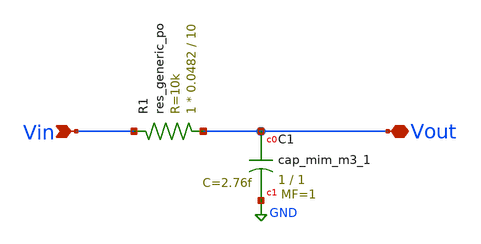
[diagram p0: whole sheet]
** sch_path: xschem/analog_desing/Filtro/LowPassFilter.sch
**.subckt LowPassFilter Vin Vout
*.ipin Vin
*.iopin Vout
XC1 Vout GND sky130_fd_pr__cap_mim_m3_1 W=1 L=1 MF=1 m=1
XR1 Vout Vin sky130_fd_pr__res_generic_po W=0.0482 L=10 m=1
**.ends
.GLOBAL GND
.end
